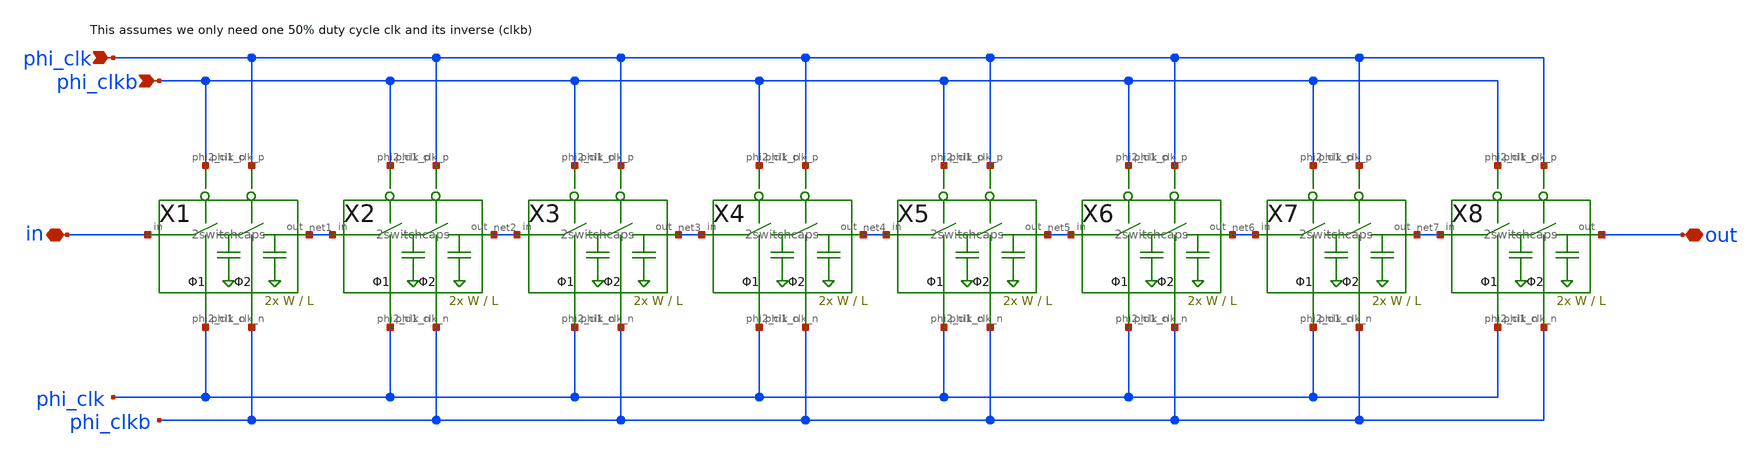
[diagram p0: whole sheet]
** sch_path: xschem/Switched_Caps/16switchcaps.sch
**.subckt 16switchcaps in out phi_clk phi_clkb
*.iopin in
*.iopin out
*.ipin phi_clk
*.ipin phi_clkb
X1 in net1 phi_clkb phi_clk phi_clkb phi_clk 2switchcaps W_C=W L_C=L
X2 net1 net2 phi_clkb phi_clk phi_clkb phi_clk 2switchcaps W_C=W L_C=L
X3 net2 net3 phi_clkb phi_clk phi_clkb phi_clk 2switchcaps W_C=W L_C=L
X4 net3 net4 phi_clkb phi_clk phi_clkb phi_clk 2switchcaps W_C=W L_C=L
X5 net4 net5 phi_clkb phi_clk phi_clkb phi_clk 2switchcaps W_C=W L_C=L
X6 net5 net6 phi_clkb phi_clk phi_clkb phi_clk 2switchcaps W_C=W L_C=L
X7 net6 net7 phi_clkb phi_clk phi_clkb phi_clk 2switchcaps W_C=W L_C=L
X8 net7 out phi_clkb phi_clk phi_clkb phi_clk 2switchcaps W_C=W L_C=L
**.ends

* expanding   symbol:  Switched_Caps/2switchcaps.sym # of pins=6
** sym_path: xschem/Switched_Caps/2switchcaps.sym
** sch_path: xschem/Switched_Caps/2switchcaps.sch
.subckt 2switchcaps in out phi2_clk_n phi1_clk_n phi1_clk_p phi2_clk_p  Wcap=20 Lcap=20
*.iopin out
*.iopin in
*.ipin phi1_clk_n
*.ipin phi1_clk_p
*.ipin phi2_clk_p
*.ipin phi2_clk_n
XC1 c1 GND sky130_fd_pr__cap_mim_m3_1 W=Wcap L=Lcap MF=1 m=1
X1 in c1 phi1_clk_p phi1_clk_n transmission_gate
X2 c1 out phi2_clk_p phi2_clk_n transmission_gate
XC2 out GND sky130_fd_pr__cap_mim_m3_1 W=Wcap L=Lcap MF=1 m=1
.ends


* expanding   symbol:  transmission_gate/transmission_gate.sym # of pins=4
** sym_path: xschem/transmission_gate/transmission_gate.sym
** sch_path: xschem/transmission_gate/transmission_gate.sch
.subckt transmission_gate in out ctrl_ ctrl
*.iopin in
*.iopin out
*.ipin ctrl_
*.ipin ctrl
XM3 in ctrl out GND sky130_fd_pr__nfet_01v8 L=0.18 W=1 nf=1 ad='int((nf+1)/2) * W/nf * 0.29' as='int((nf+2)/2) * W/nf * 0.29'
+ pd='2*int((nf+1)/2) * (W/nf + 0.29)' ps='2*int((nf+2)/2) * (W/nf + 0.29)' nrd='0.29 / W' nrs='0.29 / W'
+ sa=0 sb=0 sd=0 mult=1 m=1
XM4 out ctrl_ in VDD sky130_fd_pr__pfet_01v8 L=0.18 W=1 nf=1 ad='int((nf+1)/2) * W/nf * 0.29' as='int((nf+2)/2) * W/nf * 0.29'
+ pd='2*int((nf+1)/2) * (W/nf + 0.29)' ps='2*int((nf+2)/2) * (W/nf + 0.29)' nrd='0.29 / W' nrs='0.29 / W'
+ sa=0 sb=0 sd=0 mult=1 m=1
.ends

.GLOBAL GND
.GLOBAL VDD
.end
